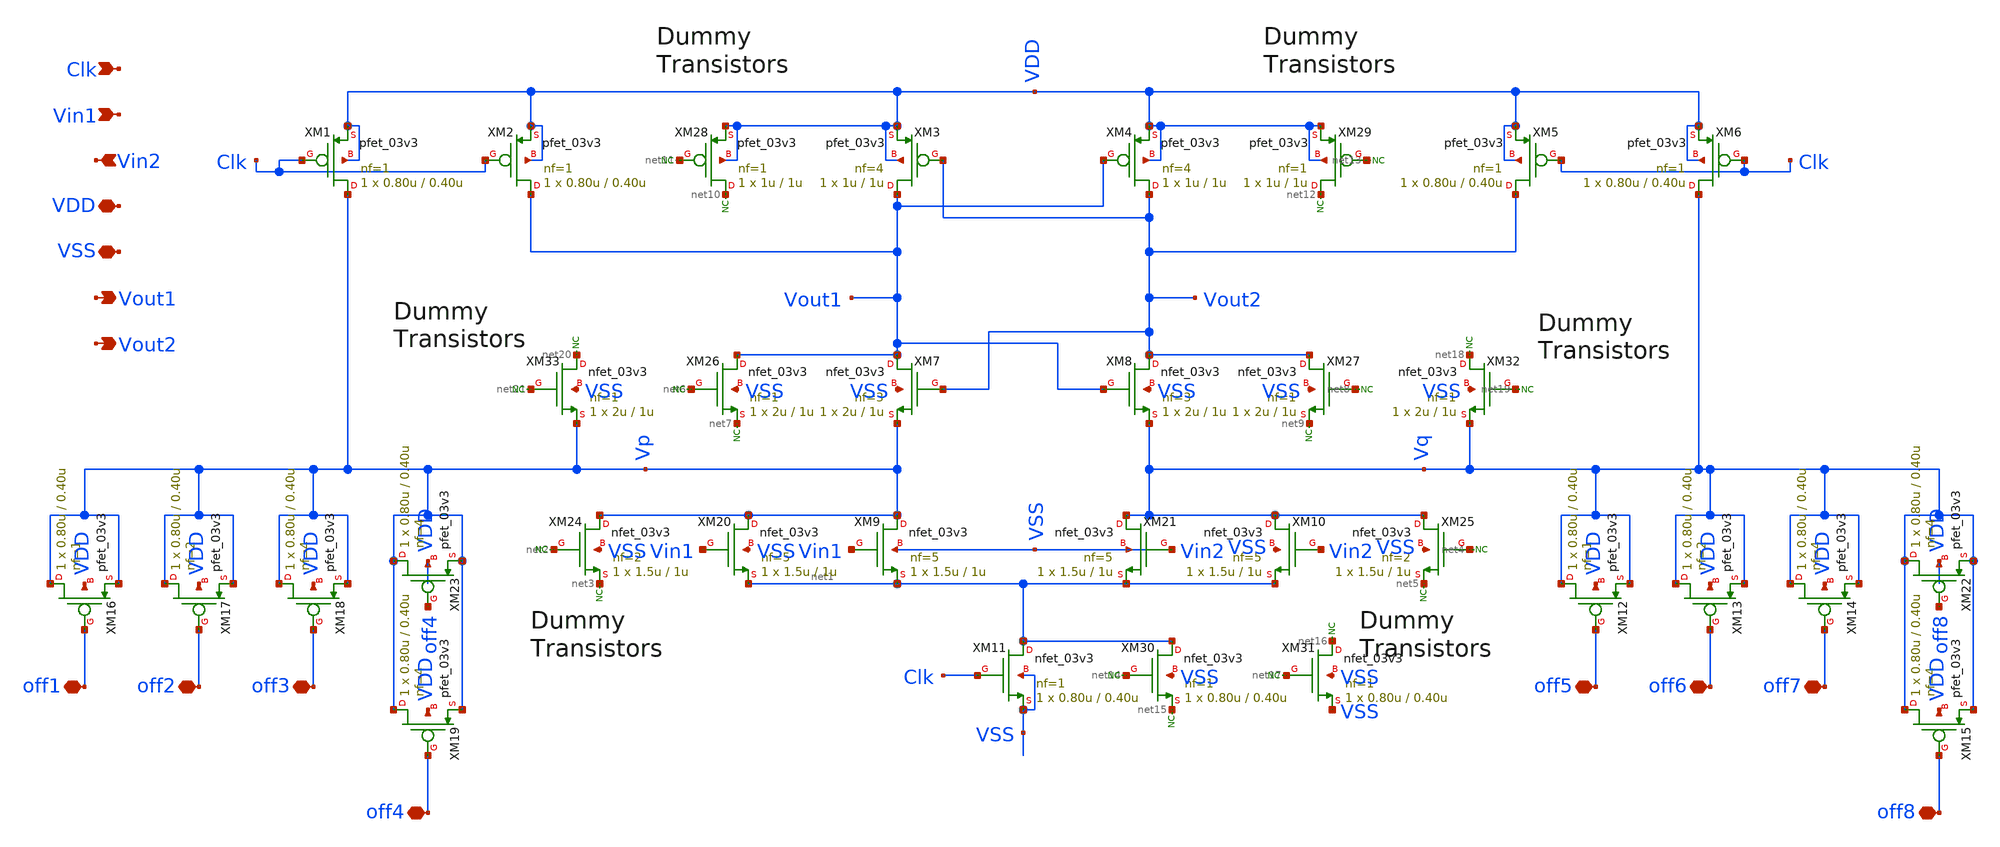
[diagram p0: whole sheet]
** sch_path: designs/comparator/final_magic/lvsclean_SAlatch/lvsclean_SAlatch.sch
**.subckt lvsclean_SAlatch Clk Vin1 Vin2 VDD VSS Vout1 Vout2 off5 off6 off7 off8 off1 off2 off3 off4
*.ipin Clk
*.ipin Vin1
*.ipin Vin2
*.iopin VDD
*.iopin VSS
*.opin Vout1
*.opin Vout2
*.iopin off5
*.iopin off6
*.iopin off7
*.iopin off8
*.iopin off1
*.iopin off2
*.iopin off3
*.iopin off4
XM1 Vp Clk VDD VDD pfet_03v3 L=0.40u W=0.80u nf=1 ad='int((nf+1)/2) * W/nf * 0.18u' as='int((nf+2)/2) * W/nf * 0.18u'
+ pd='2*int((nf+1)/2) * (W/nf + 0.18u)' ps='2*int((nf+2)/2) * (W/nf + 0.18u)' nrd='0.18u / W' nrs='0.18u / W'
+ sa=0 sb=0 sd=0 m=1
XM2 Vout1 Clk VDD VDD pfet_03v3 L=0.40u W=0.80u nf=1 ad='int((nf+1)/2) * W/nf * 0.18u' as='int((nf+2)/2) * W/nf * 0.18u'
+ pd='2*int((nf+1)/2) * (W/nf + 0.18u)' ps='2*int((nf+2)/2) * (W/nf + 0.18u)' nrd='0.18u / W' nrs='0.18u / W'
+ sa=0 sb=0 sd=0 m=1
XM3 Vout1 Vout2 VDD VDD pfet_03v3 L=1u W=1u nf=4 ad='int((nf+1)/2) * W/nf * 0.18u' as='int((nf+2)/2) * W/nf * 0.18u'
+ pd='2*int((nf+1)/2) * (W/nf + 0.18u)' ps='2*int((nf+2)/2) * (W/nf + 0.18u)' nrd='0.18u / W' nrs='0.18u / W'
+ sa=0 sb=0 sd=0 m=1
XM4 Vout2 Vout1 VDD VDD pfet_03v3 L=1u W=1u nf=4 ad='int((nf+1)/2) * W/nf * 0.18u' as='int((nf+2)/2) * W/nf * 0.18u'
+ pd='2*int((nf+1)/2) * (W/nf + 0.18u)' ps='2*int((nf+2)/2) * (W/nf + 0.18u)' nrd='0.18u / W' nrs='0.18u / W'
+ sa=0 sb=0 sd=0 m=1
XM5 Vout2 Clk VDD VDD pfet_03v3 L=0.40u W=0.80u nf=1 ad='int((nf+1)/2) * W/nf * 0.18u' as='int((nf+2)/2) * W/nf * 0.18u'
+ pd='2*int((nf+1)/2) * (W/nf + 0.18u)' ps='2*int((nf+2)/2) * (W/nf + 0.18u)' nrd='0.18u / W' nrs='0.18u / W'
+ sa=0 sb=0 sd=0 m=1
XM6 Vq Clk VDD VDD pfet_03v3 L=0.40u W=0.80u nf=1 ad='int((nf+1)/2) * W/nf * 0.18u' as='int((nf+2)/2) * W/nf * 0.18u'
+ pd='2*int((nf+1)/2) * (W/nf + 0.18u)' ps='2*int((nf+2)/2) * (W/nf + 0.18u)' nrd='0.18u / W' nrs='0.18u / W'
+ sa=0 sb=0 sd=0 m=1
XM7 Vout1 Vout2 Vp VSS nfet_03v3 L=1u W=2u nf=3 ad='int((nf+1)/2) * W/nf * 0.18u' as='int((nf+2)/2) * W/nf * 0.18u'
+ pd='2*int((nf+1)/2) * (W/nf + 0.18u)' ps='2*int((nf+2)/2) * (W/nf + 0.18u)' nrd='0.18u / W' nrs='0.18u / W'
+ sa=0 sb=0 sd=0 m=1
XM8 Vout2 Vout1 Vq VSS nfet_03v3 L=1u W=2u nf=3 ad='int((nf+1)/2) * W/nf * 0.18u' as='int((nf+2)/2) * W/nf * 0.18u'
+ pd='2*int((nf+1)/2) * (W/nf + 0.18u)' ps='2*int((nf+2)/2) * (W/nf + 0.18u)' nrd='0.18u / W' nrs='0.18u / W'
+ sa=0 sb=0 sd=0 m=1
XM9 Vp Vin1 net1 VSS nfet_03v3 L=1u W=1.5u nf=5 ad='int((nf+1)/2) * W/nf * 0.18u' as='int((nf+2)/2) * W/nf * 0.18u'
+ pd='2*int((nf+1)/2) * (W/nf + 0.18u)' ps='2*int((nf+2)/2) * (W/nf + 0.18u)' nrd='0.18u / W' nrs='0.18u / W'
+ sa=0 sb=0 sd=0 m=1
XM10 Vq Vin2 net1 VSS nfet_03v3 L=1u W=1.5u nf=5 ad='int((nf+1)/2) * W/nf * 0.18u' as='int((nf+2)/2) * W/nf * 0.18u'
+ pd='2*int((nf+1)/2) * (W/nf + 0.18u)' ps='2*int((nf+2)/2) * (W/nf + 0.18u)' nrd='0.18u / W' nrs='0.18u / W'
+ sa=0 sb=0 sd=0 m=1
XM11 net1 Clk VSS VSS nfet_03v3 L=0.40u W=0.80u nf=1 ad='int((nf+1)/2) * W/nf * 0.18u' as='int((nf+2)/2) * W/nf * 0.18u'
+ pd='2*int((nf+1)/2) * (W/nf + 0.18u)' ps='2*int((nf+2)/2) * (W/nf + 0.18u)' nrd='0.18u / W' nrs='0.18u / W'
+ sa=0 sb=0 sd=0 m=1
XM12 Vq off5 Vq VDD pfet_03v3 L=0.40u W=0.80u nf=1 ad='int((nf+1)/2) * W/nf * 0.18u' as='int((nf+2)/2) * W/nf * 0.18u'
+ pd='2*int((nf+1)/2) * (W/nf + 0.18u)' ps='2*int((nf+2)/2) * (W/nf + 0.18u)' nrd='0.18u / W' nrs='0.18u / W'
+ sa=0 sb=0 sd=0 m=1
XM13 Vq off6 Vq VDD pfet_03v3 L=0.40u W=0.80u nf=2 ad='int((nf+1)/2) * W/nf * 0.18u' as='int((nf+2)/2) * W/nf * 0.18u'
+ pd='2*int((nf+1)/2) * (W/nf + 0.18u)' ps='2*int((nf+2)/2) * (W/nf + 0.18u)' nrd='0.18u / W' nrs='0.18u / W'
+ sa=0 sb=0 sd=0 m=1
XM14 Vq off7 Vq VDD pfet_03v3 L=0.40u W=0.80u nf=4 ad='int((nf+1)/2) * W/nf * 0.18u' as='int((nf+2)/2) * W/nf * 0.18u'
+ pd='2*int((nf+1)/2) * (W/nf + 0.18u)' ps='2*int((nf+2)/2) * (W/nf + 0.18u)' nrd='0.18u / W' nrs='0.18u / W'
+ sa=0 sb=0 sd=0 m=1
XM15 Vq off8 Vq VDD pfet_03v3 L=0.40u W=0.80u nf=4 ad='int((nf+1)/2) * W/nf * 0.18u' as='int((nf+2)/2) * W/nf * 0.18u'
+ pd='2*int((nf+1)/2) * (W/nf + 0.18u)' ps='2*int((nf+2)/2) * (W/nf + 0.18u)' nrd='0.18u / W' nrs='0.18u / W'
+ sa=0 sb=0 sd=0 m=1
XM16 Vp off1 Vp VDD pfet_03v3 L=0.40u W=0.80u nf=1 ad='int((nf+1)/2) * W/nf * 0.18u' as='int((nf+2)/2) * W/nf * 0.18u'
+ pd='2*int((nf+1)/2) * (W/nf + 0.18u)' ps='2*int((nf+2)/2) * (W/nf + 0.18u)' nrd='0.18u / W' nrs='0.18u / W'
+ sa=0 sb=0 sd=0 m=1
XM17 Vp off2 Vp VDD pfet_03v3 L=0.40u W=0.80u nf=2 ad='int((nf+1)/2) * W/nf * 0.18u' as='int((nf+2)/2) * W/nf * 0.18u'
+ pd='2*int((nf+1)/2) * (W/nf + 0.18u)' ps='2*int((nf+2)/2) * (W/nf + 0.18u)' nrd='0.18u / W' nrs='0.18u / W'
+ sa=0 sb=0 sd=0 m=1
XM18 Vp off3 Vp VDD pfet_03v3 L=0.40u W=0.80u nf=4 ad='int((nf+1)/2) * W/nf * 0.18u' as='int((nf+2)/2) * W/nf * 0.18u'
+ pd='2*int((nf+1)/2) * (W/nf + 0.18u)' ps='2*int((nf+2)/2) * (W/nf + 0.18u)' nrd='0.18u / W' nrs='0.18u / W'
+ sa=0 sb=0 sd=0 m=1
XM19 Vp off4 Vp VDD pfet_03v3 L=0.40u W=0.80u nf=4 ad='int((nf+1)/2) * W/nf * 0.18u' as='int((nf+2)/2) * W/nf * 0.18u'
+ pd='2*int((nf+1)/2) * (W/nf + 0.18u)' ps='2*int((nf+2)/2) * (W/nf + 0.18u)' nrd='0.18u / W' nrs='0.18u / W'
+ sa=0 sb=0 sd=0 m=1
XM20 Vp Vin1 net1 VSS nfet_03v3 L=1u W=1.5u nf=5 ad='int((nf+1)/2) * W/nf * 0.18u' as='int((nf+2)/2) * W/nf * 0.18u'
+ pd='2*int((nf+1)/2) * (W/nf + 0.18u)' ps='2*int((nf+2)/2) * (W/nf + 0.18u)' nrd='0.18u / W' nrs='0.18u / W'
+ sa=0 sb=0 sd=0 m=1
XM21 Vq Vin2 net1 VSS nfet_03v3 L=1u W=1.5u nf=5 ad='int((nf+1)/2) * W/nf * 0.18u' as='int((nf+2)/2) * W/nf * 0.18u'
+ pd='2*int((nf+1)/2) * (W/nf + 0.18u)' ps='2*int((nf+2)/2) * (W/nf + 0.18u)' nrd='0.18u / W' nrs='0.18u / W'
+ sa=0 sb=0 sd=0 m=1
XM22 Vq off8 Vq VDD pfet_03v3 L=0.40u W=0.80u nf=4 ad='int((nf+1)/2) * W/nf * 0.18u' as='int((nf+2)/2) * W/nf * 0.18u'
+ pd='2*int((nf+1)/2) * (W/nf + 0.18u)' ps='2*int((nf+2)/2) * (W/nf + 0.18u)' nrd='0.18u / W' nrs='0.18u / W'
+ sa=0 sb=0 sd=0 m=1
XM23 Vp off4 Vp VDD pfet_03v3 L=0.40u W=0.80u nf=4 ad='int((nf+1)/2) * W/nf * 0.18u' as='int((nf+2)/2) * W/nf * 0.18u'
+ pd='2*int((nf+1)/2) * (W/nf + 0.18u)' ps='2*int((nf+2)/2) * (W/nf + 0.18u)' nrd='0.18u / W' nrs='0.18u / W'
+ sa=0 sb=0 sd=0 m=1
XM24 Vp net2 net3 VSS nfet_03v3 L=1u W=1.5u nf=2 ad='int((nf+1)/2) * W/nf * 0.18u' as='int((nf+2)/2) * W/nf * 0.18u'
+ pd='2*int((nf+1)/2) * (W/nf + 0.18u)' ps='2*int((nf+2)/2) * (W/nf + 0.18u)' nrd='0.18u / W' nrs='0.18u / W'
+ sa=0 sb=0 sd=0 m=1
* noconn #net3
* noconn #net2
XM25 Vq net4 net5 VSS nfet_03v3 L=1u W=1.5u nf=2 ad='int((nf+1)/2) * W/nf * 0.18u' as='int((nf+2)/2) * W/nf * 0.18u'
+ pd='2*int((nf+1)/2) * (W/nf + 0.18u)' ps='2*int((nf+2)/2) * (W/nf + 0.18u)' nrd='0.18u / W' nrs='0.18u / W'
+ sa=0 sb=0 sd=0 m=1
* noconn #net5
* noconn #net4
XM26 Vout1 net6 net7 VSS nfet_03v3 L=1u W=2u nf=1 ad='int((nf+1)/2) * W/nf * 0.18u' as='int((nf+2)/2) * W/nf * 0.18u'
+ pd='2*int((nf+1)/2) * (W/nf + 0.18u)' ps='2*int((nf+2)/2) * (W/nf + 0.18u)' nrd='0.18u / W' nrs='0.18u / W'
+ sa=0 sb=0 sd=0 m=1
* noconn #net7
* noconn #net6
XM27 Vout2 net8 net9 VSS nfet_03v3 L=1u W=2u nf=1 ad='int((nf+1)/2) * W/nf * 0.18u' as='int((nf+2)/2) * W/nf * 0.18u'
+ pd='2*int((nf+1)/2) * (W/nf + 0.18u)' ps='2*int((nf+2)/2) * (W/nf + 0.18u)' nrd='0.18u / W' nrs='0.18u / W'
+ sa=0 sb=0 sd=0 m=1
* noconn #net9
* noconn #net8
* noconn #net10
* noconn #net11
* noconn #net12
* noconn #net13
XM30 net1 net14 net15 VSS nfet_03v3 L=0.40u W=0.80u nf=1 ad='int((nf+1)/2) * W/nf * 0.18u' as='int((nf+2)/2) * W/nf * 0.18u'
+ pd='2*int((nf+1)/2) * (W/nf + 0.18u)' ps='2*int((nf+2)/2) * (W/nf + 0.18u)' nrd='0.18u / W' nrs='0.18u / W'
+ sa=0 sb=0 sd=0 m=1
XM31 net16 net17 VSS VSS nfet_03v3 L=0.40u W=0.80u nf=1 ad='int((nf+1)/2) * W/nf * 0.18u' as='int((nf+2)/2) * W/nf * 0.18u'
+ pd='2*int((nf+1)/2) * (W/nf + 0.18u)' ps='2*int((nf+2)/2) * (W/nf + 0.18u)' nrd='0.18u / W' nrs='0.18u / W'
+ sa=0 sb=0 sd=0 m=1
* noconn #net15
* noconn #net16
* noconn #net17
* noconn #net14
XM32 net18 net19 Vq VSS nfet_03v3 L=1u W=2u nf=1 ad='int((nf+1)/2) * W/nf * 0.18u' as='int((nf+2)/2) * W/nf * 0.18u'
+ pd='2*int((nf+1)/2) * (W/nf + 0.18u)' ps='2*int((nf+2)/2) * (W/nf + 0.18u)' nrd='0.18u / W' nrs='0.18u / W'
+ sa=0 sb=0 sd=0 m=1
* noconn #net18
* noconn #net19
XM33 net20 net21 Vp VSS nfet_03v3 L=1u W=2u nf=1 ad='int((nf+1)/2) * W/nf * 0.18u' as='int((nf+2)/2) * W/nf * 0.18u'
+ pd='2*int((nf+1)/2) * (W/nf + 0.18u)' ps='2*int((nf+2)/2) * (W/nf + 0.18u)' nrd='0.18u / W' nrs='0.18u / W'
+ sa=0 sb=0 sd=0 m=1
* noconn #net20
* noconn #net21
XM28 net10 net11 VDD VDD pfet_03v3 L=1u W=1u nf=1 ad='int((nf+1)/2) * W/nf * 0.18u' as='int((nf+2)/2) * W/nf * 0.18u'
+ pd='2*int((nf+1)/2) * (W/nf + 0.18u)' ps='2*int((nf+2)/2) * (W/nf + 0.18u)' nrd='0.18u / W' nrs='0.18u / W'
+ sa=0 sb=0 sd=0 m=1
XM29 net12 net13 VDD VDD pfet_03v3 L=1u W=1u nf=1 ad='int((nf+1)/2) * W/nf * 0.18u' as='int((nf+2)/2) * W/nf * 0.18u'
+ pd='2*int((nf+1)/2) * (W/nf + 0.18u)' ps='2*int((nf+2)/2) * (W/nf + 0.18u)' nrd='0.18u / W' nrs='0.18u / W'
+ sa=0 sb=0 sd=0 m=1
**.ends
.end
